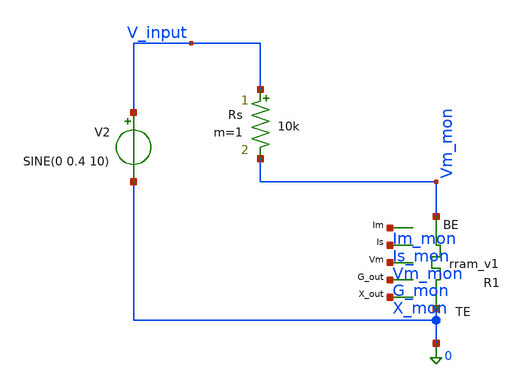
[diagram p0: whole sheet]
** sch_path: tb_monitor_comparison_2.sch
**.subckt tb_monitor_comparison_2
V2 V_input 0 SINE(0 0.4 10)
XR1 0 Vm_mon X_mon G_mon Vm_mon Is_mon Im_mon rram_v1
Rs V_input Vm_mon 10k m=1
**** begin user architecture code


*================================================================
* Simulation setup - matches Python parameters
*================================================================
.options num_threads=8
.options method=gear
.options maxstep=2u
.options reltol=1e-4
.options abstol=1e-12

* Transient analysis
.tran 2u 200m

.control
	save all
	run
	write tb_monitor_comparison.raw

	* Export data for Python comparison
	set wr_singlescale
	set wr_vecnames
	option numdgt=15
	wrdata /home/salieri/eda/designs/Capibara_tuto/MEMS/tmp/spice_results.txt time v(V_input) v(Vm_mon)
+ v(X_mon) v(G_mon) v(Im_mon) v(Is_mon) i(v2)
.endc



*================================================================
* RRAM Model with Internal Variable Monitoring
*================================================================

.control
pre_osdi /foss/designs/Capibara_tuto/MEMS/rram_v1_with_monitors.osdi
.endc

*----------------------------------------------------------------
* Subcircuit with monitoring outputs
*----------------------------------------------------------------
.subckt rram_v1 TE BE X_OUT G_OUT VM_OUT IS_OUT IM_OUT
N1 TE BE X_OUT G_OUT VM_OUT IS_OUT IM_OUT rram_v1_model
.ends rram_v1

*----------------------------------------------------------------
* Model parameters (match Python exactly)
*----------------------------------------------------------------
.model rram_v1_model rram_v1_va   x0=0.0  Ron=13e3  Roff=460e3  tau=6e-5  T=108.5  Von_threshold=0.2
+  Voff=-0.1  phi=0.88  Af=1e-7  Ar=1e-7  Bf=8  Br=8

**** end user architecture code
**.ends
.end
